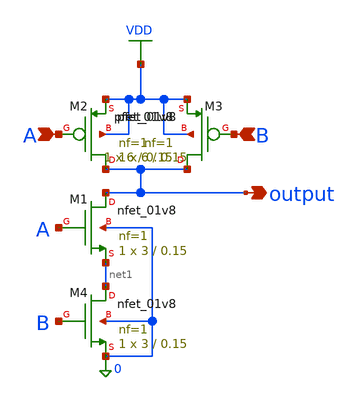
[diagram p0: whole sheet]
** sch_path: nand2.sch
**.subckt nand2 output A B
*.opin output
*.ipin A
*.ipin B
XM1 output A net1 0 sky130_fd_pr__nfet_01v8 L=0.15 W=3 nf=1 ad='int((1 + 1)/2) * 3 / 1 * 0.29' as='int((1 + 2)/2) * 3 / 1 * 0.29'
+ pd='2*int((1 + 1)/2) * (3 / 1 + 0.29)' ps='2*int((1 + 2)/2) * (3 / 1 + 0.29)' nrd='0.29 / 3 ' nrs='0.29 / 3 '
+ sa=0 sb=0 sd=0 mult=1 m=1
XM2 output A VDD VDD sky130_fd_pr__pfet_01v8 L=0.15 W=6 nf=1 ad='int((1 + 1)/2) * 6 / 1 * 0.29' as='int((1 + 2)/2) * 6 / 1 * 0.29'
+ pd='2*int((1 + 1)/2) * (6 / 1 + 0.29)' ps='2*int((1 + 2)/2) * (6 / 1 + 0.29)' nrd='0.29 / 6 ' nrs='0.29 / 6 '
+ sa=0 sb=0 sd=0 mult=1 m=1
XM3 output B VDD VDD sky130_fd_pr__pfet_01v8 L=0.15 W=6 nf=1 ad='int((1 + 1)/2) * 6 / 1 * 0.29' as='int((1 + 2)/2) * 6 / 1 * 0.29'
+ pd='2*int((1 + 1)/2) * (6 / 1 + 0.29)' ps='2*int((1 + 2)/2) * (6 / 1 + 0.29)' nrd='0.29 / 6 ' nrs='0.29 / 6 '
+ sa=0 sb=0 sd=0 mult=1 m=1
XM4 net1 B 0 0 sky130_fd_pr__nfet_01v8 L=0.15 W=3 nf=1 ad='int((1 + 1)/2) * 3 / 1 * 0.29' as='int((1 + 2)/2) * 3 / 1 * 0.29'
+ pd='2*int((1 + 1)/2) * (3 / 1 + 0.29)' ps='2*int((1 + 2)/2) * (3 / 1 + 0.29)' nrd='0.29 / 3 ' nrs='0.29 / 3 '
+ sa=0 sb=0 sd=0 mult=1 m=1
**.ends
.GLOBAL VDD
.end
